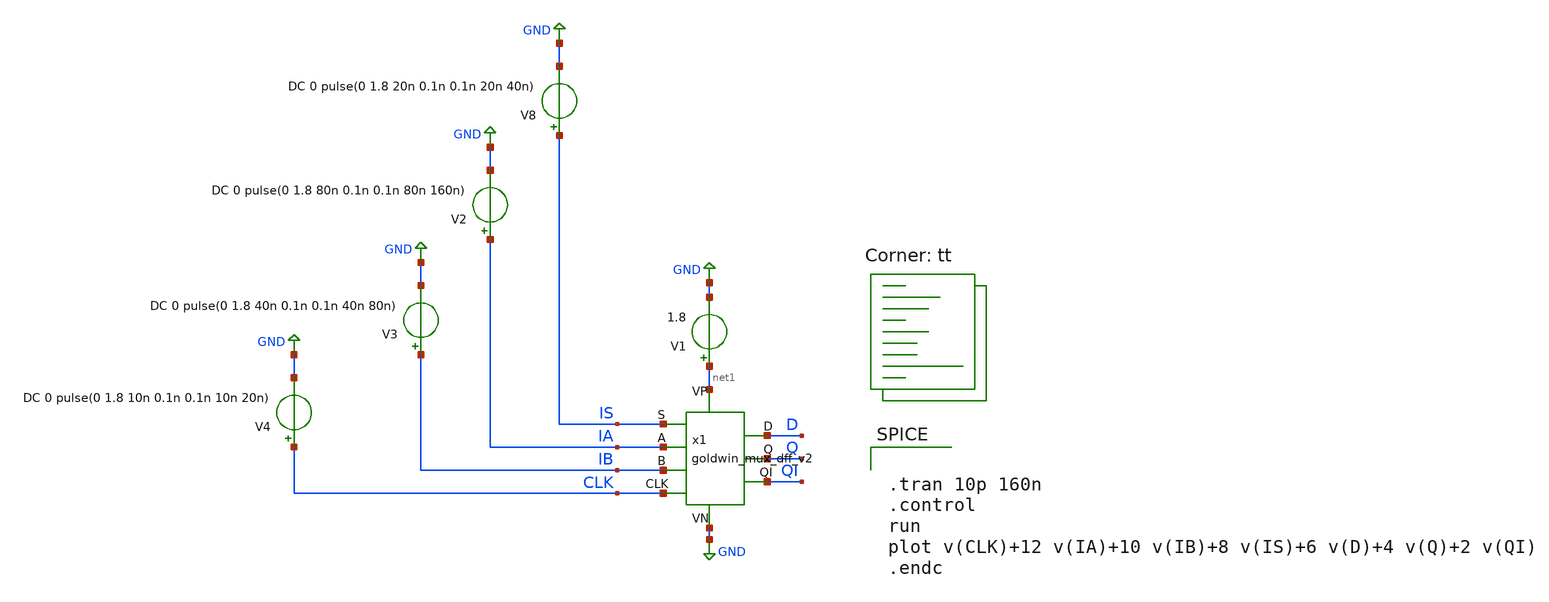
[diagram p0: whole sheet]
** sch_path: APIC-UTS/schematic/goldwin_mux_dff_v2/tb_goldwin_mux_dff_v2.sch
**.subckt tb_goldwin_mux_dff_v2
V8 IS GND DC 0 pulse(0 1.8 20n 0.1n 0.1n 20n 40n)
V2 IA GND DC 0 pulse(0 1.8 80n 0.1n 0.1n 80n 160n)
V3 IB GND DC 0 pulse(0 1.8 40n 0.1n 0.1n 40n 80n)
V4 CLK GND DC 0 pulse(0 1.8 10n 0.1n 0.1n 10n 20n)
V1 net1 GND 1.8
x1 CLK IA IB IS D Q QI net1 GND goldwin_mux_dff_v2
**** begin user architecture code


.tran 10p 160n
.control
run
plot v(CLK)+12 v(IA)+10 v(IB)+8 v(IS)+6 v(D)+4 v(Q)+2 v(QI)
.endc


.lib $::SKYWATER_MODELS/sky130.lib.spice tt
**** end user architecture code
**.ends
.GLOBAL GND
.end
